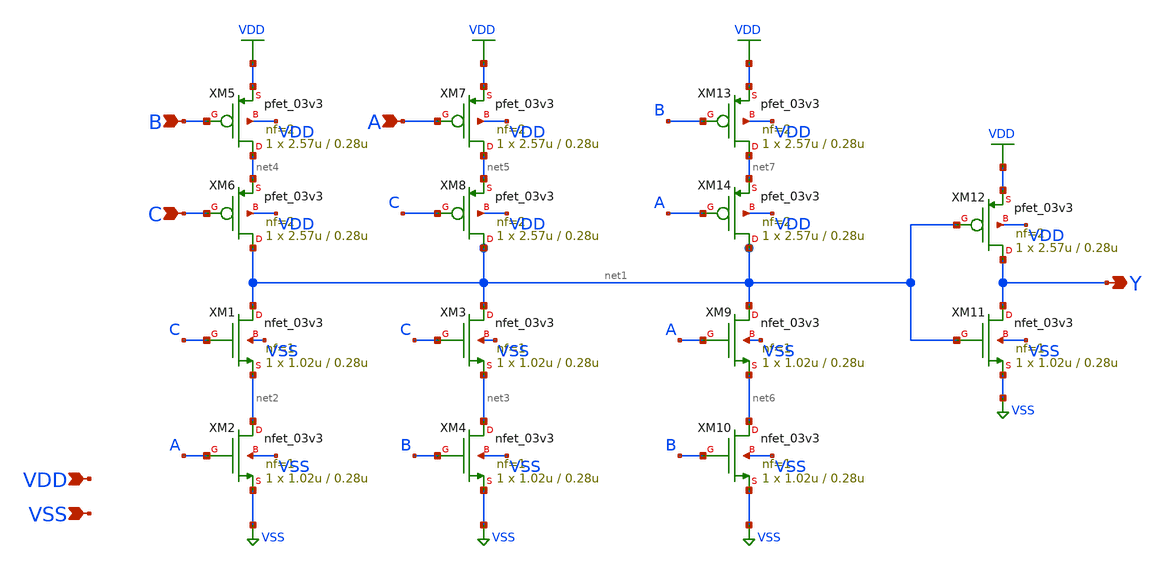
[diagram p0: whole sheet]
** sch_path: xschem/gf180mcu_ocd_sc_rt12t3v3__maj3_1.sch
**.subckt gf180mcu_ocd_sc_rt12t3v3__maj3_1 A B C Y VDD VSS
*.ipin A
*.ipin B
*.ipin C
*.opin Y
*.ipin VDD
*.ipin VSS
XM1 net1 C net2 VSS nfet_03v3 L=0.28u W=1.02u nf=1 ad='int((nf+1)/2) * W/nf * 0.18u' as='int((nf+2)/2) * W/nf * 0.18u'
+ pd='2*int((nf+1)/2) * (W/nf + 0.18u)' ps='2*int((nf+2)/2) * (W/nf + 0.18u)' nrd='0.18u / W' nrs='0.18u / W'
+ sa=0 sb=0 sd=0 m=1
XM2 net2 A VSS VSS nfet_03v3 L=0.28u W=1.02u nf=1 ad='int((nf+1)/2) * W/nf * 0.18u' as='int((nf+2)/2) * W/nf * 0.18u'
+ pd='2*int((nf+1)/2) * (W/nf + 0.18u)' ps='2*int((nf+2)/2) * (W/nf + 0.18u)' nrd='0.18u / W' nrs='0.18u / W'
+ sa=0 sb=0 sd=0 m=1
XM3 net1 C net3 VSS nfet_03v3 L=0.28u W=1.02u nf=1 ad='int((nf+1)/2) * W/nf * 0.18u' as='int((nf+2)/2) * W/nf * 0.18u'
+ pd='2*int((nf+1)/2) * (W/nf + 0.18u)' ps='2*int((nf+2)/2) * (W/nf + 0.18u)' nrd='0.18u / W' nrs='0.18u / W'
+ sa=0 sb=0 sd=0 m=1
XM4 net3 B VSS VSS nfet_03v3 L=0.28u W=1.02u nf=1 ad='int((nf+1)/2) * W/nf * 0.18u' as='int((nf+2)/2) * W/nf * 0.18u'
+ pd='2*int((nf+1)/2) * (W/nf + 0.18u)' ps='2*int((nf+2)/2) * (W/nf + 0.18u)' nrd='0.18u / W' nrs='0.18u / W'
+ sa=0 sb=0 sd=0 m=1
XM5 net4 B VDD VDD pfet_03v3 L=0.28u W=2.57u nf=2 ad='int((nf+1)/2) * W/nf * 0.18u' as='int((nf+2)/2) * W/nf * 0.18u'
+ pd='2*int((nf+1)/2) * (W/nf + 0.18u)' ps='2*int((nf+2)/2) * (W/nf + 0.18u)' nrd='0.18u / W' nrs='0.18u / W'
+ sa=0 sb=0 sd=0 m=1
XM6 net1 C net4 VDD pfet_03v3 L=0.28u W=2.57u nf=2 ad='int((nf+1)/2) * W/nf * 0.18u' as='int((nf+2)/2) * W/nf * 0.18u'
+ pd='2*int((nf+1)/2) * (W/nf + 0.18u)' ps='2*int((nf+2)/2) * (W/nf + 0.18u)' nrd='0.18u / W' nrs='0.18u / W'
+ sa=0 sb=0 sd=0 m=1
XM7 net5 A VDD VDD pfet_03v3 L=0.28u W=2.57u nf=2 ad='int((nf+1)/2) * W/nf * 0.18u' as='int((nf+2)/2) * W/nf * 0.18u'
+ pd='2*int((nf+1)/2) * (W/nf + 0.18u)' ps='2*int((nf+2)/2) * (W/nf + 0.18u)' nrd='0.18u / W' nrs='0.18u / W'
+ sa=0 sb=0 sd=0 m=1
XM8 net1 C net5 VDD pfet_03v3 L=0.28u W=2.57u nf=2 ad='int((nf+1)/2) * W/nf * 0.18u' as='int((nf+2)/2) * W/nf * 0.18u'
+ pd='2*int((nf+1)/2) * (W/nf + 0.18u)' ps='2*int((nf+2)/2) * (W/nf + 0.18u)' nrd='0.18u / W' nrs='0.18u / W'
+ sa=0 sb=0 sd=0 m=1
XM11 Y net1 VSS VSS nfet_03v3 L=0.28u W=1.02u nf=1 ad='int((nf+1)/2) * W/nf * 0.18u' as='int((nf+2)/2) * W/nf * 0.18u'
+ pd='2*int((nf+1)/2) * (W/nf + 0.18u)' ps='2*int((nf+2)/2) * (W/nf + 0.18u)' nrd='0.18u / W' nrs='0.18u / W'
+ sa=0 sb=0 sd=0 m=1
XM12 Y net1 VDD VDD pfet_03v3 L=0.28u W=2.57u nf=2 ad='int((nf+1)/2) * W/nf * 0.18u' as='int((nf+2)/2) * W/nf * 0.18u'
+ pd='2*int((nf+1)/2) * (W/nf + 0.18u)' ps='2*int((nf+2)/2) * (W/nf + 0.18u)' nrd='0.18u / W' nrs='0.18u / W'
+ sa=0 sb=0 sd=0 m=1
XM9 net1 A net6 VSS nfet_03v3 L=0.28u W=1.02u nf=1 ad='int((nf+1)/2) * W/nf * 0.18u' as='int((nf+2)/2) * W/nf * 0.18u'
+ pd='2*int((nf+1)/2) * (W/nf + 0.18u)' ps='2*int((nf+2)/2) * (W/nf + 0.18u)' nrd='0.18u / W' nrs='0.18u / W'
+ sa=0 sb=0 sd=0 m=1
XM10 net6 B VSS VSS nfet_03v3 L=0.28u W=1.02u nf=1 ad='int((nf+1)/2) * W/nf * 0.18u' as='int((nf+2)/2) * W/nf * 0.18u'
+ pd='2*int((nf+1)/2) * (W/nf + 0.18u)' ps='2*int((nf+2)/2) * (W/nf + 0.18u)' nrd='0.18u / W' nrs='0.18u / W'
+ sa=0 sb=0 sd=0 m=1
XM13 net7 B VDD VDD pfet_03v3 L=0.28u W=2.57u nf=2 ad='int((nf+1)/2) * W/nf * 0.18u' as='int((nf+2)/2) * W/nf * 0.18u'
+ pd='2*int((nf+1)/2) * (W/nf + 0.18u)' ps='2*int((nf+2)/2) * (W/nf + 0.18u)' nrd='0.18u / W' nrs='0.18u / W'
+ sa=0 sb=0 sd=0 m=1
XM14 net1 A net7 VDD pfet_03v3 L=0.28u W=2.57u nf=2 ad='int((nf+1)/2) * W/nf * 0.18u' as='int((nf+2)/2) * W/nf * 0.18u'
+ pd='2*int((nf+1)/2) * (W/nf + 0.18u)' ps='2*int((nf+2)/2) * (W/nf + 0.18u)' nrd='0.18u / W' nrs='0.18u / W'
+ sa=0 sb=0 sd=0 m=1
**.ends
.GLOBAL VSS
.GLOBAL VDD
.end
